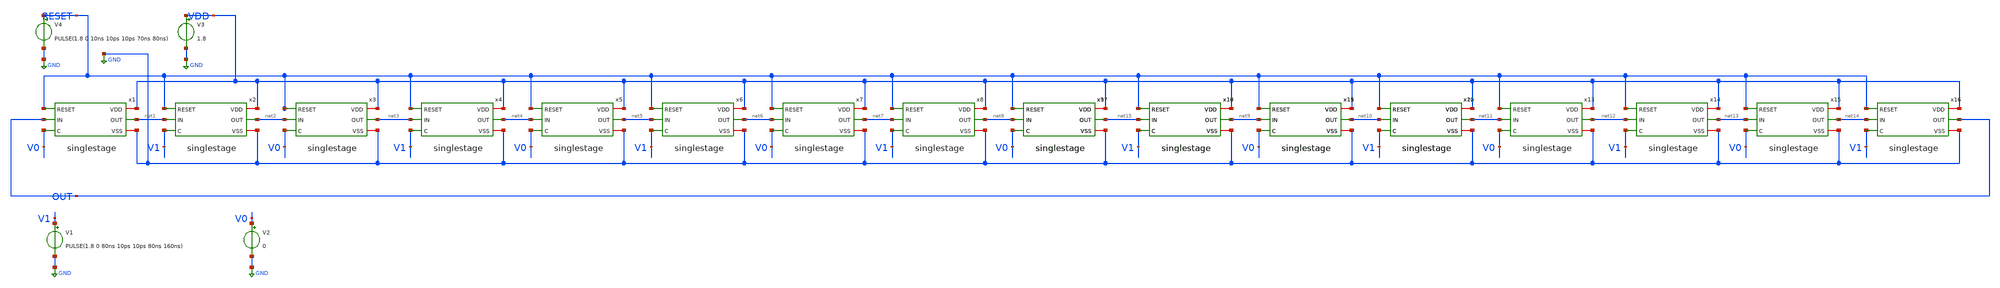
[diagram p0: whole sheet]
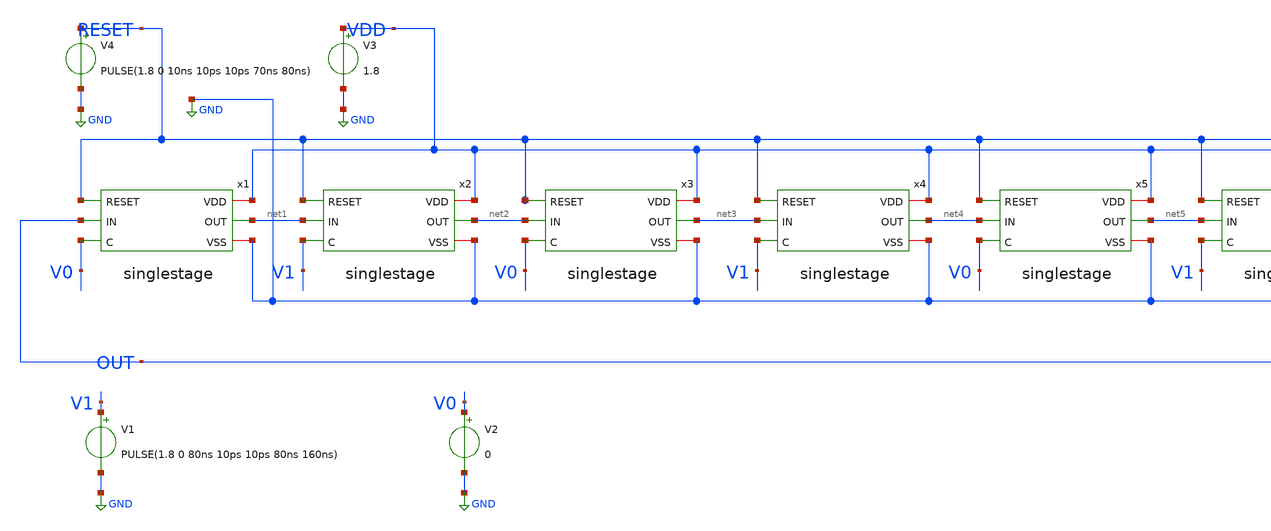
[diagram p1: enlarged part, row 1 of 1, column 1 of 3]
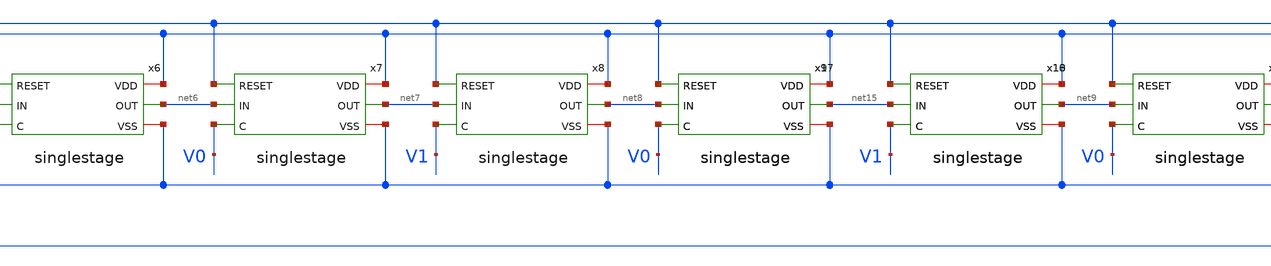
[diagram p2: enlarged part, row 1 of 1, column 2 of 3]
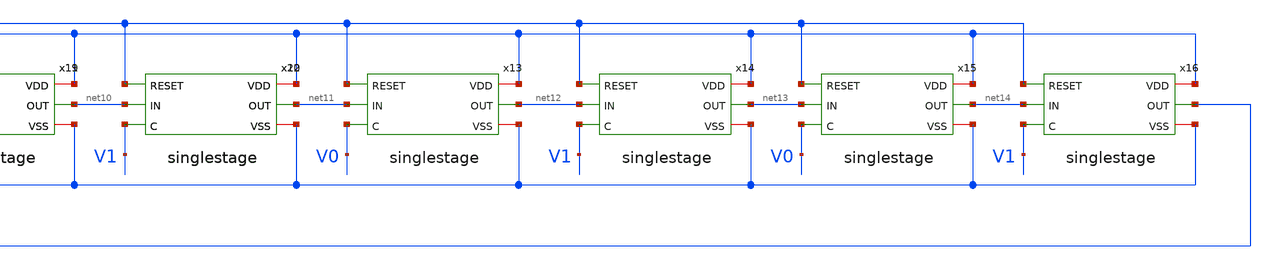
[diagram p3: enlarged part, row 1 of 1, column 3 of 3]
** sch_path: xiaolin/16cell.sch
**.subckt 16cell
x1 RESET VDD GND net1 OUT V0 singlestage
x2 RESET VDD GND net2 net1 V1 singlestage
x3 RESET VDD GND net3 net2 V0 singlestage
x4 RESET VDD GND net4 net3 V1 singlestage
x5 RESET VDD GND net5 net4 V0 singlestage
x6 RESET VDD GND net6 net5 V1 singlestage
x7 RESET VDD GND net7 net6 V0 singlestage
x8 RESET VDD GND net8 net7 V1 singlestage
x9 RESET VDD GND net15 net8 V0 singlestage
x10 RESET VDD GND net9 net15 V1 singlestage
x11 RESET VDD GND net10 net9 V0 singlestage
x12 RESET VDD GND net11 net10 V1 singlestage
x13 RESET VDD GND net12 net11 V0 singlestage
x14 RESET VDD GND net13 net12 V1 singlestage
x15 RESET VDD GND net14 net13 V0 singlestage
x16 RESET VDD GND OUT net14 V1 singlestage
x17 RESET VDD GND net15 net8 V0 singlestage
x18 RESET VDD GND net9 net15 V1 singlestage
x19 RESET VDD GND net10 net9 V0 singlestage
x20 RESET VDD GND net11 net10 V1 singlestage
V1 V1 GND PULSE(1.8 0 80ns 10ps 10ps 80ns 160ns)
V2 V0 GND 0
V3 VDD GND 1.8
V4 RESET GND PULSE(1.8 0 10ns 10ps 10ps 70ns 80ns)
**** begin user architecture code

** opencircuitdesign pdks install
**.lib $::SKYWATER_MODELS/sky130.lib.spice tt
.lib /farmshare/home/classes/ee/372/PDKs/open_pdks/sky130/sky130A/libs.tech/ngspice/sky130.lib.spice tt
.include /farmshare/home/classes/ee/372/PDKs/open_pdks/sky130/sky130A/libs.ref/sky130_fd_sc_hd/spice/sky130_fd_sc_hd.spice





.control
save all
tran 10n 160n
.endc


**** end user architecture code
**.ends

* expanding   symbol:  singlestage.sym # of pins=6
** sym_path: design/singlestage.sym
** sch_path: design/singlestage.sch
.subckt singlestage RESET VDD VSS OUT IN C
*.ipin IN
*.ipin C
*.ipin RESET
*.iopin VSS
*.iopin VDD
*.opin OUT
x1 RESET net1 VSS VSS VDD VDD net3 sky130_fd_sc_hd__nor2_1
x2 RESET net2 VSS VSS VDD VDD net4 sky130_fd_sc_hd__nor2_1
x3 net6 VSS net1 VDD IN net5 net2 demux2-1
x4 net6 VSS net3 VDD OUT net5 net4 mux2-1
x5 net5 VSS VSS VDD VDD net6 sky130_fd_sc_hd__inv_1
XM1 net1 net6 VDD VDD sky130_fd_pr__pfet_01v8_hvt L=0.15 W=1 nf=1 ad='int((nf+1)/2) * W/nf * 0.29' as='int((nf+2)/2) * W/nf * 0.29'
+ pd='2*int((nf+1)/2) * (W/nf + 0.29)' ps='2*int((nf+2)/2) * (W/nf + 0.29)' nrd='0.29 / W' nrs='0.29 / W'
+ sa=0 sb=0 sd=0 mult=1 m=1
XM2 net2 net5 VDD VDD sky130_fd_pr__pfet_01v8_hvt L=0.15 W=1 nf=1 ad='int((nf+1)/2) * W/nf * 0.29' as='int((nf+2)/2) * W/nf * 0.29'
+ pd='2*int((nf+1)/2) * (W/nf + 0.29)' ps='2*int((nf+2)/2) * (W/nf + 0.29)' nrd='0.29 / W' nrs='0.29 / W'
+ sa=0 sb=0 sd=0 mult=1 m=1
x6 C VSS VSS VDD VDD net5 sky130_fd_sc_hd__inv_1
.ends


* expanding   symbol:  demux2-1.sym # of pins=7
** sym_path: xiaolin/demux2-1.sym
** sch_path: xiaolin/demux2-1.sch
.subckt demux2-1 S VSS OUT1 VDD IN Sbar OUT2
*.ipin Sbar
*.ipin S
*.iopin VSS
*.iopin VDD
*.opin OUT1
*.opin OUT2
*.ipin IN
XM2 IN S OUT1 VSS sky130_fd_pr__nfet_01v8 L=0.15 W=0.65 nf=1 ad='int((nf+1)/2) * W/nf * 0.29' as='int((nf+2)/2) * W/nf * 0.29'
+ pd='2*int((nf+1)/2) * (W/nf + 0.29)' ps='2*int((nf+2)/2) * (W/nf + 0.29)' nrd='0.29 / W' nrs='0.29 / W'
+ sa=0 sb=0 sd=0 mult=1 m=1
XM1 IN Sbar OUT2 VSS sky130_fd_pr__nfet_01v8 L=0.15 W=0.65 nf=1 ad='int((nf+1)/2) * W/nf * 0.29' as='int((nf+2)/2) * W/nf * 0.29'
+ pd='2*int((nf+1)/2) * (W/nf + 0.29)' ps='2*int((nf+2)/2) * (W/nf + 0.29)' nrd='0.29 / W' nrs='0.29 / W'
+ sa=0 sb=0 sd=0 mult=1 m=1
XM3 IN S OUT2 VDD sky130_fd_pr__pfet_01v8_hvt L=0.15 W=1 nf=1 ad='int((nf+1)/2) * W/nf * 0.29' as='int((nf+2)/2) * W/nf * 0.29'
+ pd='2*int((nf+1)/2) * (W/nf + 0.29)' ps='2*int((nf+2)/2) * (W/nf + 0.29)' nrd='0.29 / W' nrs='0.29 / W'
+ sa=0 sb=0 sd=0 mult=1 m=1
XM4 IN Sbar OUT1 VDD sky130_fd_pr__pfet_01v8_hvt L=0.15 W=1 nf=1 ad='int((nf+1)/2) * W/nf * 0.29' as='int((nf+2)/2) * W/nf * 0.29'
+ pd='2*int((nf+1)/2) * (W/nf + 0.29)' ps='2*int((nf+2)/2) * (W/nf + 0.29)' nrd='0.29 / W' nrs='0.29 / W'
+ sa=0 sb=0 sd=0 mult=1 m=1
XM5 IN S OUT2 VDD sky130_fd_pr__pfet_01v8_hvt L=0.15 W=1 nf=1 ad='int((nf+1)/2) * W/nf * 0.29' as='int((nf+2)/2) * W/nf * 0.29'
+ pd='2*int((nf+1)/2) * (W/nf + 0.29)' ps='2*int((nf+2)/2) * (W/nf + 0.29)' nrd='0.29 / W' nrs='0.29 / W'
+ sa=0 sb=0 sd=0 mult=1 m=1
.ends


* expanding   symbol:  mux2-1.sym # of pins=7
** sym_path: design/mux2-1.sym
** sch_path: design/mux2-1.sch
.subckt mux2-1 S VSS IN1 VDD OUT Sbar IN2
*.ipin IN1
*.ipin IN2
*.ipin Sbar
*.ipin S
*.opin OUT
*.iopin VSS
*.iopin VDD
XM2 IN1 S OUT VSS sky130_fd_pr__nfet_01v8 L=0.15 W=0.65 nf=1 ad='int((nf+1)/2) * W/nf * 0.29' as='int((nf+2)/2) * W/nf * 0.29'
+ pd='2*int((nf+1)/2) * (W/nf + 0.29)' ps='2*int((nf+2)/2) * (W/nf + 0.29)' nrd='0.29 / W' nrs='0.29 / W'
+ sa=0 sb=0 sd=0 mult=1 m=1
XM1 IN2 Sbar OUT VSS sky130_fd_pr__nfet_01v8 L=0.15 W=0.65 nf=1 ad='int((nf+1)/2) * W/nf * 0.29' as='int((nf+2)/2) * W/nf * 0.29'
+ pd='2*int((nf+1)/2) * (W/nf + 0.29)' ps='2*int((nf+2)/2) * (W/nf + 0.29)' nrd='0.29 / W' nrs='0.29 / W'
+ sa=0 sb=0 sd=0 mult=1 m=1
XM4 IN1 Sbar OUT VDD sky130_fd_pr__pfet_01v8_hvt L=0.15 W=1 nf=1 ad='int((nf+1)/2) * W/nf * 0.29' as='int((nf+2)/2) * W/nf * 0.29'
+ pd='2*int((nf+1)/2) * (W/nf + 0.29)' ps='2*int((nf+2)/2) * (W/nf + 0.29)' nrd='0.29 / W' nrs='0.29 / W'
+ sa=0 sb=0 sd=0 mult=1 m=1
XM5 IN2 S OUT VDD sky130_fd_pr__pfet_01v8_hvt L=0.15 W=1 nf=1 ad='int((nf+1)/2) * W/nf * 0.29' as='int((nf+2)/2) * W/nf * 0.29'
+ pd='2*int((nf+1)/2) * (W/nf + 0.29)' ps='2*int((nf+2)/2) * (W/nf + 0.29)' nrd='0.29 / W' nrs='0.29 / W'
+ sa=0 sb=0 sd=0 mult=1 m=1
.ends

.GLOBAL GND
.end
